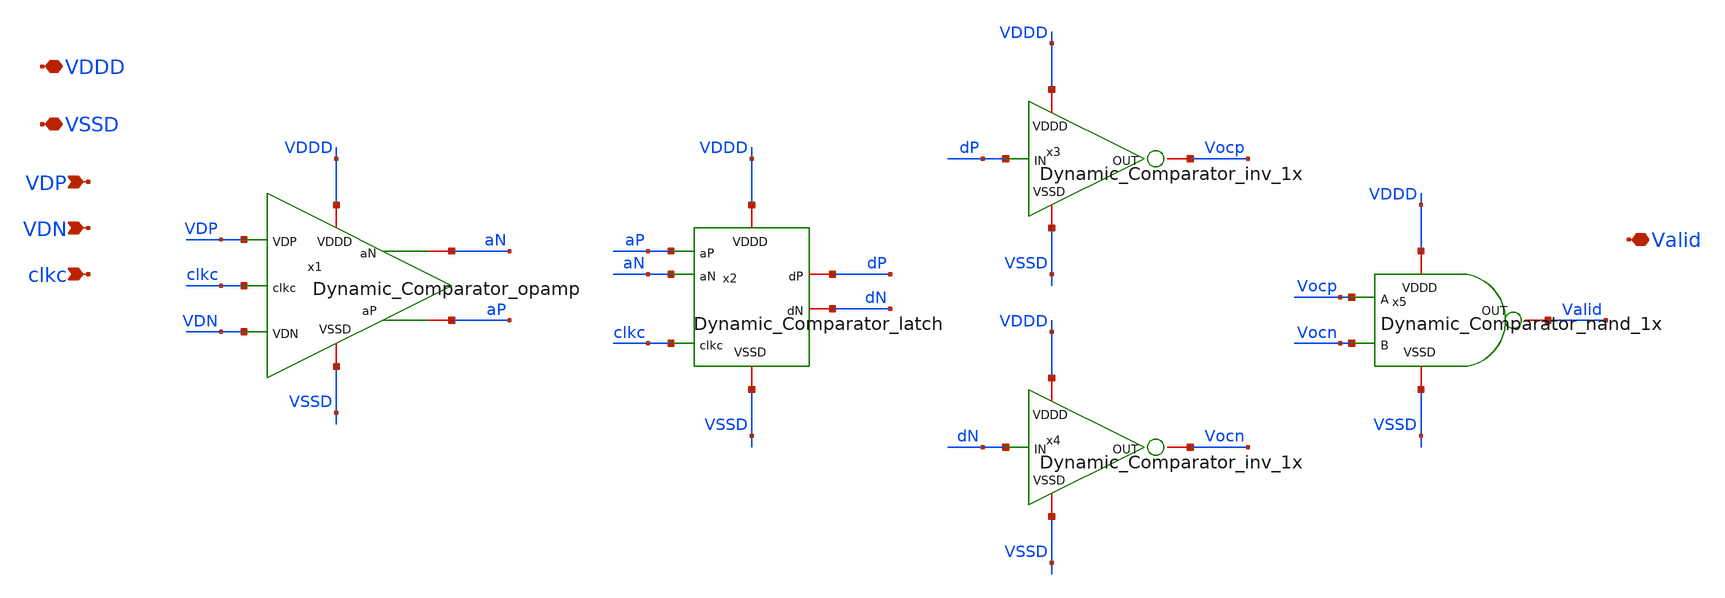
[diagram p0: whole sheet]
** sch_path: SAR_ADC/blocks/Dynamic_Comparator/Dynamic_Comparator.sch
**.subckt Dynamic_Comparator VDDD VSSD VDP VDN clkc Valid
*.iopin VDDD
*.iopin VSSD
*.ipin VDP
*.ipin VDN
*.ipin clkc
*.iopin Valid
x1 aN VDDD aP VSSD clkc VDP VDN Dynamic_Comparator_opamp
x2 VDDD VSSD dN clkc dP aP aN Dynamic_Comparator_latch
x3 VDDD VSSD Vocp dP Dynamic_Comparator_inv_1x
x4 VDDD VSSD Vocn dN Dynamic_Comparator_inv_1x
x5 VDDD VSSD Valid Vocp Vocn Dynamic_Comparator_nand_1x
**.ends
.end
